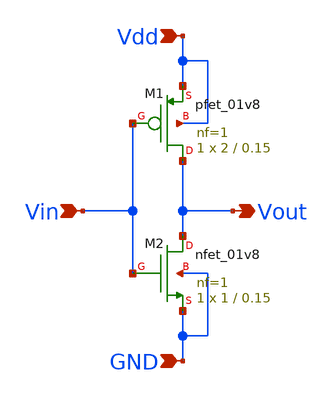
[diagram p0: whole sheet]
** sch_path: inv.sch
**.subckt inv Vin Vout Vdd GND
*.ipin Vin
*.opin Vout
*.ipin Vdd
*.ipin GND
XM1 Vout Vin Vdd Vdd sky130_fd_pr__pfet_01v8 L=0.15 W=2 nf=1 ad='int((nf+1)/2) * W/nf * 0.29' as='int((nf+2)/2) * W/nf * 0.29'
+ pd='2*int((nf+1)/2) * (W/nf + 0.29)' ps='2*int((nf+2)/2) * (W/nf + 0.29)' nrd='0.29 / W' nrs='0.29 / W'
+ sa=0 sb=0 sd=0 mult=1 m=1
XM2 Vout Vin GND GND sky130_fd_pr__nfet_01v8 L=0.15 W=1 nf=1 ad='int((nf+1)/2) * W/nf * 0.29' as='int((nf+2)/2) * W/nf * 0.29'
+ pd='2*int((nf+1)/2) * (W/nf + 0.29)' ps='2*int((nf+2)/2) * (W/nf + 0.29)' nrd='0.29 / W' nrs='0.29 / W'
+ sa=0 sb=0 sd=0 mult=1 m=1
**.ends
.end
